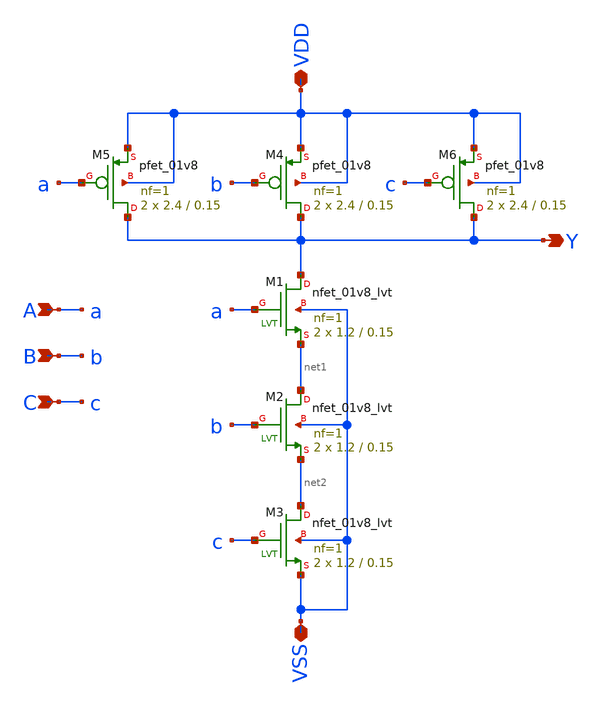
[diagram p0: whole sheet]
** sch_path: xschem_lib/sylee21/nand_3.sch
**.subckt nand_3 VDD Y VSS A B C
*.iopin VDD
*.opin Y
*.iopin VSS
*.ipin A
*.ipin B
*.ipin C
XM1 Y a net1 VSS sky130_fd_pr__nfet_01v8_lvt L=0.15 W=1.2 nf=1 ad='int((nf+1)/2) * W/nf * 0.29' as='int((nf+2)/2) * W/nf * 0.29'
+ pd='2*int((nf+1)/2) * (W/nf + 0.29)' ps='2*int((nf+2)/2) * (W/nf + 0.29)' nrd='0.29 / W' nrs='0.29 / W'
+ sa=0 sb=0 sd=0 mult=2 m=2
XM2 net1 b net2 VSS sky130_fd_pr__nfet_01v8_lvt L=0.15 W=1.2 nf=1 ad='int((nf+1)/2) * W/nf * 0.29' as='int((nf+2)/2) * W/nf * 0.29'
+ pd='2*int((nf+1)/2) * (W/nf + 0.29)' ps='2*int((nf+2)/2) * (W/nf + 0.29)' nrd='0.29 / W' nrs='0.29 / W'
+ sa=0 sb=0 sd=0 mult=2 m=2
XM3 net2 c VSS VSS sky130_fd_pr__nfet_01v8_lvt L=0.15 W=1.2 nf=1 ad='int((nf+1)/2) * W/nf * 0.29' as='int((nf+2)/2) * W/nf * 0.29'
+ pd='2*int((nf+1)/2) * (W/nf + 0.29)' ps='2*int((nf+2)/2) * (W/nf + 0.29)' nrd='0.29 / W' nrs='0.29 / W'
+ sa=0 sb=0 sd=0 mult=2 m=2
XM4 Y b VDD VDD sky130_fd_pr__pfet_01v8 L=0.15 W=2.4 nf=1 ad='int((nf+1)/2) * W/nf * 0.29' as='int((nf+2)/2) * W/nf * 0.29'
+ pd='2*int((nf+1)/2) * (W/nf + 0.29)' ps='2*int((nf+2)/2) * (W/nf + 0.29)' nrd='0.29 / W' nrs='0.29 / W'
+ sa=0 sb=0 sd=0 mult=2 m=2
XM5 Y a VDD VDD sky130_fd_pr__pfet_01v8 L=0.15 W=2.4 nf=1 ad='int((nf+1)/2) * W/nf * 0.29' as='int((nf+2)/2) * W/nf * 0.29'
+ pd='2*int((nf+1)/2) * (W/nf + 0.29)' ps='2*int((nf+2)/2) * (W/nf + 0.29)' nrd='0.29 / W' nrs='0.29 / W'
+ sa=0 sb=0 sd=0 mult=2 m=2
XM6 Y c VDD VDD sky130_fd_pr__pfet_01v8 L=0.15 W=2.4 nf=1 ad='int((nf+1)/2) * W/nf * 0.29' as='int((nf+2)/2) * W/nf * 0.29'
+ pd='2*int((nf+1)/2) * (W/nf + 0.29)' ps='2*int((nf+2)/2) * (W/nf + 0.29)' nrd='0.29 / W' nrs='0.29 / W'
+ sa=0 sb=0 sd=0 mult=2 m=2
**.ends
.end
